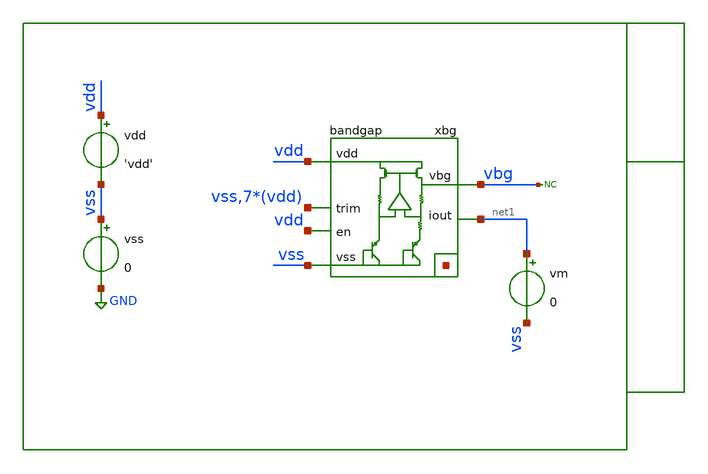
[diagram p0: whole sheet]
** sch_path: xschem/tb/bandgap_cm/bandgap/op_bandgap.sch
**.subckt op_bandgap
xbg vdd vbg vss net2[7] net2[6] net2[5] net2[4] net2[3] net2[2] net2[1] net2[0] vss vdd vdd vdd vdd
+ vdd vdd vdd net1 vdd bandgap
vdd vdd vss 'vdd'
vss vss GND 0
* noconn vbg
vm net1 vss 0
**** begin user architecture code

* Control

.param vdd = 3.3

.temp 27

.options reltol  = 1e-6
.options abstol  = 1e-12
.options gmin    = 1e-15

*------------------------------------------------------------
* Nodeset for better convergence
*------------------------------------------------------------
.nodeset v(vbg)  = '1'
.nodeset v(xbg.gate) = 'vdd/2'
.nodeset v(xbg.vx)   = '0.70'
.nodeset v(xbg.vbe2) = '0.65'
.nodeset v(xbg.vs1)  = '0'
*------------------------------------------------------------


.control

save all

* optran 0 0 0 100n 0.3m 0
op

let gm_xbg_xm2 = @m.xbg.xm2.m0[gm]
let gm_xbg_xms1 = @m.xbg.xms1.m0[gm]
let gm_xbg_xm1 = @m.xbg.xm1.m0[gm]
let gm_xbg_xmo1 = @m.xbg.xmo1.m0[gm]
let gm_xbg_xmb1 = @m.xbg.xmb1.m0[gm]
let gm_xbg_xmb2 = @m.xbg.xmb2.m0[gm]
let gm_xbg_xmb3 = @m.xbg.xmb3.m0[gm]
let gm_xbg_xmb2 = @m.xbg.xmb2.m0[gm]
let gm_xbg_xmb3 = @m.xbg.xmb3.m0[gm]
let gm_xbg_xmo2 = @m.xbg.xmo2.m0[gm]
let gm_xbg_xme1 = @m.xbg.xme1.m0[gm]
let gm_xbg_xme2 = @m.xbg.xme2.m0[gm]
let gm_xbg_xmi2 = @m.xbg.xmi2.m0[gm]
let gm_xbg_xmi1 = @m.xbg.xmi1.m0[gm]
let gm_xbg_xme3 = @m.xbg.xme3.m0[gm]
let gm_xbg_xme4 = @m.xbg.xme4.m0[gm]
let gm_xbg_xms2 = @m.xbg.xms2.m0[gm]
let gm_xbg_xms3 = @m.xbg.xms3.m0[gm]
let gm_xbg_xms4 = @m.xbg.xms4.m0[gm]
let gm_xamp_xmb1 = @m.xbg.xamp.xmb1.m0[gm]
let gm_xamp_xmb3 = @m.xbg.xamp.xmb3.m0[gm]
let gm_xamp_xmb2 = @m.xbg.xamp.xmb2.m0[gm]
let gm_xamp_xmd1 = @m.xbg.xamp.xmd1.m0[gm]
let gm_xamp_xmb4 = @m.xbg.xamp.xmb4.m0[gm]
let gm_xamp_xmb5 = @m.xbg.xamp.xmb5.m0[gm]
let gm_xamp_xmd2 = @m.xbg.xamp.xmd2.m0[gm]
let gm_xamp_xmt1 = @m.xbg.xamp.xmt1.m0[gm]
let gm_xamp_xmc7 = @m.xbg.xamp.xmc7.m0[gm]
let gm_xamp_xmc8 = @m.xbg.xamp.xmc8.m0[gm]
let gm_xamp_xmc1 = @m.xbg.xamp.xmc1.m0[gm]
let gm_xamp_xmc2 = @m.xbg.xamp.xmc2.m0[gm]
let gm_xamp_xmc3 = @m.xbg.xamp.xmc3.m0[gm]
let gm_xamp_xmc4 = @m.xbg.xamp.xmc4.m0[gm]
let gm_xamp_xmc5 = @m.xbg.xamp.xmc5.m0[gm]
let gm_xamp_xmc6 = @m.xbg.xamp.xmc6.m0[gm]
let gds_xbg_xm2 = @m.xbg.xm2.m0[gds]
let gds_xbg_xms1 = @m.xbg.xms1.m0[gds]
let gds_xbg_xm1 = @m.xbg.xm1.m0[gds]
let gds_xbg_xmo1 = @m.xbg.xmo1.m0[gds]
let gds_xbg_xmb1 = @m.xbg.xmb1.m0[gds]
let gds_xbg_xmb2 = @m.xbg.xmb2.m0[gds]
let gds_xbg_xmb3 = @m.xbg.xmb3.m0[gds]
let gds_xbg_xmb2 = @m.xbg.xmb2.m0[gds]
let gds_xbg_xmb3 = @m.xbg.xmb3.m0[gds]
let gds_xbg_xmo2 = @m.xbg.xmo2.m0[gds]
let gds_xbg_xme1 = @m.xbg.xme1.m0[gds]
let gds_xbg_xme2 = @m.xbg.xme2.m0[gds]
let gds_xbg_xmi2 = @m.xbg.xmi2.m0[gds]
let gds_xbg_xmi1 = @m.xbg.xmi1.m0[gds]
let gds_xbg_xme3 = @m.xbg.xme3.m0[gds]
let gds_xbg_xme4 = @m.xbg.xme4.m0[gds]
let gds_xbg_xms2 = @m.xbg.xms2.m0[gds]
let gds_xbg_xms3 = @m.xbg.xms3.m0[gds]
let gds_xbg_xms4 = @m.xbg.xms4.m0[gds]
let gds_xamp_xmb1 = @m.xbg.xamp.xmb1.m0[gds]
let gds_xamp_xmb3 = @m.xbg.xamp.xmb3.m0[gds]
let gds_xamp_xmb2 = @m.xbg.xamp.xmb2.m0[gds]
let gds_xamp_xmd1 = @m.xbg.xamp.xmd1.m0[gds]
let gds_xamp_xmb4 = @m.xbg.xamp.xmb4.m0[gds]
let gds_xamp_xmb5 = @m.xbg.xamp.xmb5.m0[gds]
let gds_xamp_xmd2 = @m.xbg.xamp.xmd2.m0[gds]
let gds_xamp_xmt1 = @m.xbg.xamp.xmt1.m0[gds]
let gds_xamp_xmc7 = @m.xbg.xamp.xmc7.m0[gds]
let gds_xamp_xmc8 = @m.xbg.xamp.xmc8.m0[gds]
let gds_xamp_xmc1 = @m.xbg.xamp.xmc1.m0[gds]
let gds_xamp_xmc2 = @m.xbg.xamp.xmc2.m0[gds]
let gds_xamp_xmc3 = @m.xbg.xamp.xmc3.m0[gds]
let gds_xamp_xmc4 = @m.xbg.xamp.xmc4.m0[gds]
let gds_xamp_xmc5 = @m.xbg.xamp.xmc5.m0[gds]
let gds_xamp_xmc6 = @m.xbg.xamp.xmc6.m0[gds]
let vdsat_xbg_xm2 = @m.xbg.xm2.m0[vdsat]
let vdsat_xbg_xms1 = @m.xbg.xms1.m0[vdsat]
let vdsat_xbg_xm1 = @m.xbg.xm1.m0[vdsat]
let vdsat_xbg_xmo1 = @m.xbg.xmo1.m0[vdsat]
let vdsat_xbg_xmb1 = @m.xbg.xmb1.m0[vdsat]
let vdsat_xbg_xmb2 = @m.xbg.xmb2.m0[vdsat]
let vdsat_xbg_xmb3 = @m.xbg.xmb3.m0[vdsat]
let vdsat_xbg_xmb2 = @m.xbg.xmb2.m0[vdsat]
let vdsat_xbg_xmb3 = @m.xbg.xmb3.m0[vdsat]
let vdsat_xbg_xmo2 = @m.xbg.xmo2.m0[vdsat]
let vdsat_xbg_xme1 = @m.xbg.xme1.m0[vdsat]
let vdsat_xbg_xme2 = @m.xbg.xme2.m0[vdsat]
let vdsat_xbg_xmi2 = @m.xbg.xmi2.m0[vdsat]
let vdsat_xbg_xmi1 = @m.xbg.xmi1.m0[vdsat]
let vdsat_xbg_xme3 = @m.xbg.xme3.m0[vdsat]
let vdsat_xbg_xme4 = @m.xbg.xme4.m0[vdsat]
let vdsat_xbg_xms2 = @m.xbg.xms2.m0[vdsat]
let vdsat_xbg_xms3 = @m.xbg.xms3.m0[vdsat]
let vdsat_xbg_xms4 = @m.xbg.xms4.m0[vdsat]
let vdsat_xamp_xmb1 = @m.xbg.xamp.xmb1.m0[vdsat]
let vdsat_xamp_xmb3 = @m.xbg.xamp.xmb3.m0[vdsat]
let vdsat_xamp_xmb2 = @m.xbg.xamp.xmb2.m0[vdsat]
let vdsat_xamp_xmd1 = @m.xbg.xamp.xmd1.m0[vdsat]
let vdsat_xamp_xmb4 = @m.xbg.xamp.xmb4.m0[vdsat]
let vdsat_xamp_xmb5 = @m.xbg.xamp.xmb5.m0[vdsat]
let vdsat_xamp_xmd2 = @m.xbg.xamp.xmd2.m0[vdsat]
let vdsat_xamp_xmt1 = @m.xbg.xamp.xmt1.m0[vdsat]
let vdsat_xamp_xmc7 = @m.xbg.xamp.xmc7.m0[vdsat]
let vdsat_xamp_xmc8 = @m.xbg.xamp.xmc8.m0[vdsat]
let vdsat_xamp_xmc1 = @m.xbg.xamp.xmc1.m0[vdsat]
let vdsat_xamp_xmc2 = @m.xbg.xamp.xmc2.m0[vdsat]
let vdsat_xamp_xmc3 = @m.xbg.xamp.xmc3.m0[vdsat]
let vdsat_xamp_xmc4 = @m.xbg.xamp.xmc4.m0[vdsat]
let vdsat_xamp_xmc5 = @m.xbg.xamp.xmc5.m0[vdsat]
let vdsat_xamp_xmc6 = @m.xbg.xamp.xmc6.m0[vdsat]
let vth_xbg_xm2 = @m.xbg.xm2.m0[vth]
let vth_xbg_xms1 = @m.xbg.xms1.m0[vth]
let vth_xbg_xm1 = @m.xbg.xm1.m0[vth]
let vth_xbg_xmo1 = @m.xbg.xmo1.m0[vth]
let vth_xbg_xmb1 = @m.xbg.xmb1.m0[vth]
let vth_xbg_xmb2 = @m.xbg.xmb2.m0[vth]
let vth_xbg_xmb3 = @m.xbg.xmb3.m0[vth]
let vth_xbg_xmb2 = @m.xbg.xmb2.m0[vth]
let vth_xbg_xmb3 = @m.xbg.xmb3.m0[vth]
let vth_xbg_xmo2 = @m.xbg.xmo2.m0[vth]
let vth_xbg_xme1 = @m.xbg.xme1.m0[vth]
let vth_xbg_xme2 = @m.xbg.xme2.m0[vth]
let vth_xbg_xmi2 = @m.xbg.xmi2.m0[vth]
let vth_xbg_xmi1 = @m.xbg.xmi1.m0[vth]
let vth_xbg_xme3 = @m.xbg.xme3.m0[vth]
let vth_xbg_xme4 = @m.xbg.xme4.m0[vth]
let vth_xbg_xms2 = @m.xbg.xms2.m0[vth]
let vth_xbg_xms3 = @m.xbg.xms3.m0[vth]
let vth_xbg_xms4 = @m.xbg.xms4.m0[vth]
let vth_xamp_xmb1 = @m.xbg.xamp.xmb1.m0[vth]
let vth_xamp_xmb3 = @m.xbg.xamp.xmb3.m0[vth]
let vth_xamp_xmb2 = @m.xbg.xamp.xmb2.m0[vth]
let vth_xamp_xmd1 = @m.xbg.xamp.xmd1.m0[vth]
let vth_xamp_xmb4 = @m.xbg.xamp.xmb4.m0[vth]
let vth_xamp_xmb5 = @m.xbg.xamp.xmb5.m0[vth]
let vth_xamp_xmd2 = @m.xbg.xamp.xmd2.m0[vth]
let vth_xamp_xmt1 = @m.xbg.xamp.xmt1.m0[vth]
let vth_xamp_xmc7 = @m.xbg.xamp.xmc7.m0[vth]
let vth_xamp_xmc8 = @m.xbg.xamp.xmc8.m0[vth]
let vth_xamp_xmc1 = @m.xbg.xamp.xmc1.m0[vth]
let vth_xamp_xmc2 = @m.xbg.xamp.xmc2.m0[vth]
let vth_xamp_xmc3 = @m.xbg.xamp.xmc3.m0[vth]
let vth_xamp_xmc4 = @m.xbg.xamp.xmc4.m0[vth]
let vth_xamp_xmc5 = @m.xbg.xamp.xmc5.m0[vth]
let vth_xamp_xmc6 = @m.xbg.xamp.xmc6.m0[vth]
let id_xbg_xm2 = @m.xbg.xm2.m0[id]
let id_xbg_xms1 = @m.xbg.xms1.m0[id]
let id_xbg_xm1 = @m.xbg.xm1.m0[id]
let id_xbg_xmo1 = @m.xbg.xmo1.m0[id]
let id_xbg_xmb1 = @m.xbg.xmb1.m0[id]
let id_xbg_xmb2 = @m.xbg.xmb2.m0[id]
let id_xbg_xmb3 = @m.xbg.xmb3.m0[id]
let id_xbg_xmb2 = @m.xbg.xmb2.m0[id]
let id_xbg_xmb3 = @m.xbg.xmb3.m0[id]
let id_xbg_xmo2 = @m.xbg.xmo2.m0[id]
let id_xbg_xme1 = @m.xbg.xme1.m0[id]
let id_xbg_xme2 = @m.xbg.xme2.m0[id]
let id_xbg_xmi2 = @m.xbg.xmi2.m0[id]
let id_xbg_xmi1 = @m.xbg.xmi1.m0[id]
let id_xbg_xme3 = @m.xbg.xme3.m0[id]
let id_xbg_xme4 = @m.xbg.xme4.m0[id]
let id_xbg_xms2 = @m.xbg.xms2.m0[id]
let id_xbg_xms3 = @m.xbg.xms3.m0[id]
let id_xbg_xms4 = @m.xbg.xms4.m0[id]
let id_xamp_xmb1 = @m.xbg.xamp.xmb1.m0[id]
let id_xamp_xmb3 = @m.xbg.xamp.xmb3.m0[id]
let id_xamp_xmb2 = @m.xbg.xamp.xmb2.m0[id]
let id_xamp_xmd1 = @m.xbg.xamp.xmd1.m0[id]
let id_xamp_xmb4 = @m.xbg.xamp.xmb4.m0[id]
let id_xamp_xmb5 = @m.xbg.xamp.xmb5.m0[id]
let id_xamp_xmd2 = @m.xbg.xamp.xmd2.m0[id]
let id_xamp_xmt1 = @m.xbg.xamp.xmt1.m0[id]
let id_xamp_xmc7 = @m.xbg.xamp.xmc7.m0[id]
let id_xamp_xmc8 = @m.xbg.xamp.xmc8.m0[id]
let id_xamp_xmc1 = @m.xbg.xamp.xmc1.m0[id]
let id_xamp_xmc2 = @m.xbg.xamp.xmc2.m0[id]
let id_xamp_xmc3 = @m.xbg.xamp.xmc3.m0[id]
let id_xamp_xmc4 = @m.xbg.xamp.xmc4.m0[id]
let id_xamp_xmc5 = @m.xbg.xamp.xmc5.m0[id]
let id_xamp_xmc6 = @m.xbg.xamp.xmc6.m0[id]
let vgs_xbg_xm2 = @m.xbg.xm2.m0[vgs]
let vgs_xbg_xms1 = @m.xbg.xms1.m0[vgs]
let vgs_xbg_xm1 = @m.xbg.xm1.m0[vgs]
let vgs_xbg_xmo1 = @m.xbg.xmo1.m0[vgs]
let vgs_xbg_xmb1 = @m.xbg.xmb1.m0[vgs]
let vgs_xbg_xmb2 = @m.xbg.xmb2.m0[vgs]
let vgs_xbg_xmb3 = @m.xbg.xmb3.m0[vgs]
let vgs_xbg_xmb2 = @m.xbg.xmb2.m0[vgs]
let vgs_xbg_xmb3 = @m.xbg.xmb3.m0[vgs]
let vgs_xbg_xmo2 = @m.xbg.xmo2.m0[vgs]
let vgs_xbg_xme1 = @m.xbg.xme1.m0[vgs]
let vgs_xbg_xme2 = @m.xbg.xme2.m0[vgs]
let vgs_xbg_xmi2 = @m.xbg.xmi2.m0[vgs]
let vgs_xbg_xmi1 = @m.xbg.xmi1.m0[vgs]
let vgs_xbg_xme3 = @m.xbg.xme3.m0[vgs]
let vgs_xbg_xme4 = @m.xbg.xme4.m0[vgs]
let vgs_xbg_xms2 = @m.xbg.xms2.m0[vgs]
let vgs_xbg_xms3 = @m.xbg.xms3.m0[vgs]
let vgs_xbg_xms4 = @m.xbg.xms4.m0[vgs]
let vgs_xamp_xmb1 = @m.xbg.xamp.xmb1.m0[vgs]
let vgs_xamp_xmb3 = @m.xbg.xamp.xmb3.m0[vgs]
let vgs_xamp_xmb2 = @m.xbg.xamp.xmb2.m0[vgs]
let vgs_xamp_xmd1 = @m.xbg.xamp.xmd1.m0[vgs]
let vgs_xamp_xmb4 = @m.xbg.xamp.xmb4.m0[vgs]
let vgs_xamp_xmb5 = @m.xbg.xamp.xmb5.m0[vgs]
let vgs_xamp_xmd2 = @m.xbg.xamp.xmd2.m0[vgs]
let vgs_xamp_xmt1 = @m.xbg.xamp.xmt1.m0[vgs]
let vgs_xamp_xmc7 = @m.xbg.xamp.xmc7.m0[vgs]
let vgs_xamp_xmc8 = @m.xbg.xamp.xmc8.m0[vgs]
let vgs_xamp_xmc1 = @m.xbg.xamp.xmc1.m0[vgs]
let vgs_xamp_xmc2 = @m.xbg.xamp.xmc2.m0[vgs]
let vgs_xamp_xmc3 = @m.xbg.xamp.xmc3.m0[vgs]
let vgs_xamp_xmc4 = @m.xbg.xamp.xmc4.m0[vgs]
let vgs_xamp_xmc5 = @m.xbg.xamp.xmc5.m0[vgs]
let vgs_xamp_xmc6 = @m.xbg.xamp.xmc6.m0[vgs]
let vds_xbg_xm2 = @m.xbg.xm2.m0[vds]
let vds_xbg_xms1 = @m.xbg.xms1.m0[vds]
let vds_xbg_xm1 = @m.xbg.xm1.m0[vds]
let vds_xbg_xmo1 = @m.xbg.xmo1.m0[vds]
let vds_xbg_xmb1 = @m.xbg.xmb1.m0[vds]
let vds_xbg_xmb2 = @m.xbg.xmb2.m0[vds]
let vds_xbg_xmb3 = @m.xbg.xmb3.m0[vds]
let vds_xbg_xmb2 = @m.xbg.xmb2.m0[vds]
let vds_xbg_xmb3 = @m.xbg.xmb3.m0[vds]
let vds_xbg_xmo2 = @m.xbg.xmo2.m0[vds]
let vds_xbg_xme1 = @m.xbg.xme1.m0[vds]
let vds_xbg_xme2 = @m.xbg.xme2.m0[vds]
let vds_xbg_xmi2 = @m.xbg.xmi2.m0[vds]
let vds_xbg_xmi1 = @m.xbg.xmi1.m0[vds]
let vds_xbg_xme3 = @m.xbg.xme3.m0[vds]
let vds_xbg_xme4 = @m.xbg.xme4.m0[vds]
let vds_xbg_xms2 = @m.xbg.xms2.m0[vds]
let vds_xbg_xms3 = @m.xbg.xms3.m0[vds]
let vds_xbg_xms4 = @m.xbg.xms4.m0[vds]
let vds_xamp_xmb1 = @m.xbg.xamp.xmb1.m0[vds]
let vds_xamp_xmb3 = @m.xbg.xamp.xmb3.m0[vds]
let vds_xamp_xmb2 = @m.xbg.xamp.xmb2.m0[vds]
let vds_xamp_xmd1 = @m.xbg.xamp.xmd1.m0[vds]
let vds_xamp_xmb4 = @m.xbg.xamp.xmb4.m0[vds]
let vds_xamp_xmb5 = @m.xbg.xamp.xmb5.m0[vds]
let vds_xamp_xmd2 = @m.xbg.xamp.xmd2.m0[vds]
let vds_xamp_xmt1 = @m.xbg.xamp.xmt1.m0[vds]
let vds_xamp_xmc7 = @m.xbg.xamp.xmc7.m0[vds]
let vds_xamp_xmc8 = @m.xbg.xamp.xmc8.m0[vds]
let vds_xamp_xmc1 = @m.xbg.xamp.xmc1.m0[vds]
let vds_xamp_xmc2 = @m.xbg.xamp.xmc2.m0[vds]
let vds_xamp_xmc3 = @m.xbg.xamp.xmc3.m0[vds]
let vds_xamp_xmc4 = @m.xbg.xamp.xmc4.m0[vds]
let vds_xamp_xmc5 = @m.xbg.xamp.xmc5.m0[vds]
let vds_xamp_xmc6 = @m.xbg.xamp.xmc6.m0[vds]

let vsat_xbg_xm2  = vds_xbg_xm2  - vdsat_xbg_xm2
let vsat_xbg_xms1 = vds_xbg_xms1 - vdsat_xbg_xms1
let vsat_xbg_xm1  = vds_xbg_xm1  - vdsat_xbg_xm1
let vsat_xbg_xmo1 = vds_xbg_xmo1 - vdsat_xbg_xmo1
let vsat_xbg_xmb1 = vds_xbg_xmb1 - vdsat_xbg_xmb1
let vsat_xbg_xmb2 = vds_xbg_xmb2 - vdsat_xbg_xmb2
let vsat_xbg_xmb3 = vds_xbg_xmb3 - vdsat_xbg_xmb3
let vsat_xbg_xmb2 = vds_xbg_xmb2 - vdsat_xbg_xmb2
let vsat_xbg_xmb3 = vds_xbg_xmb3 - vdsat_xbg_xmb3
let vsat_xbg_xmo2 = vds_xbg_xmo2 - vdsat_xbg_xmo2
let vsat_xbg_xme1 = vds_xbg_xme1 - vdsat_xbg_xme1
let vsat_xbg_xme2 = vds_xbg_xme2 - vdsat_xbg_xme2
let vsat_xbg_xmi2 = vds_xbg_xmi2 - vdsat_xbg_xmi2
let vsat_xbg_xmi1 = vds_xbg_xmi1 - vdsat_xbg_xmi1
let vsat_xbg_xme3 = vds_xbg_xme3 - vdsat_xbg_xme3
let vsat_xbg_xme4 = vds_xbg_xme4 - vdsat_xbg_xme4
let vsat_xbg_xms2 = vds_xbg_xms2 - vdsat_xbg_xms2
let vsat_xbg_xms3 = vds_xbg_xms3 - vdsat_xbg_xms3
let vsat_xbg_xms4 = vds_xbg_xms4 - vdsat_xbg_xms4
let vsat_xamp_xmb1 = vds_xamp_xmb1 - vdsat_xamp_xmb1
let vsat_xamp_xmb3 = vds_xamp_xmb3 - vdsat_xamp_xmb3
let vsat_xamp_xmb2 = vds_xamp_xmb2 - vdsat_xamp_xmb2
let vsat_xamp_xmd1 = vds_xamp_xmd1 - vdsat_xamp_xmd1
let vsat_xamp_xmb4 = vds_xamp_xmb4 - vdsat_xamp_xmb4
let vsat_xamp_xmb5 = vds_xamp_xmb5 - vdsat_xamp_xmb5
let vsat_xamp_xmd2 = vds_xamp_xmd2 - vdsat_xamp_xmd2
let vsat_xamp_xmt1 = vds_xamp_xmt1 - vdsat_xamp_xmt1
let vsat_xamp_xmc7 = vds_xamp_xmc7 - vdsat_xamp_xmc7
let vsat_xamp_xmc8 = vds_xamp_xmc8 - vdsat_xamp_xmc8
let vsat_xamp_xmc1 = vds_xamp_xmc1 - vdsat_xamp_xmc1
let vsat_xamp_xmc2 = vds_xamp_xmc2 - vdsat_xamp_xmc2
let vsat_xamp_xmc3 = vds_xamp_xmc3 - vdsat_xamp_xmc3
let vsat_xamp_xmc4 = vds_xamp_xmc4 - vdsat_xamp_xmc4
let vsat_xamp_xmc5 = vds_xamp_xmc5 - vdsat_xamp_xmc5
let vsat_xamp_xmc6 = vds_xamp_xmc6 - vdsat_xamp_xmc6

let vov_xbg_xm2  = vgs_xbg_xm2  - vth_xbg_xm2
let vov_xbg_xms1 = vgs_xbg_xms1 - vth_xbg_xms1
let vov_xbg_xm1  = vgs_xbg_xm1  - vth_xbg_xm1
let vov_xbg_xmo1 = vgs_xbg_xmo1 - vth_xbg_xmo1
let vov_xbg_xmb1 = vgs_xbg_xmb1 - vth_xbg_xmb1
let vov_xbg_xmb2 = vgs_xbg_xmb2 - vth_xbg_xmb2
let vov_xbg_xmb3 = vgs_xbg_xmb3 - vth_xbg_xmb3
let vov_xbg_xmb2 = vgs_xbg_xmb2 - vth_xbg_xmb2
let vov_xbg_xmb3 = vgs_xbg_xmb3 - vth_xbg_xmb3
let vov_xbg_xmo2 = vgs_xbg_xmo2 - vth_xbg_xmo2
let vov_xbg_xme1 = vgs_xbg_xme1 - vth_xbg_xme1
let vov_xbg_xme2 = vgs_xbg_xme2 - vth_xbg_xme2
let vov_xbg_xmi2 = vgs_xbg_xmi2 - vth_xbg_xmi2
let vov_xbg_xmi1 = vgs_xbg_xmi1 - vth_xbg_xmi1
let vov_xbg_xme3 = vgs_xbg_xme3 - vth_xbg_xme3
let vov_xbg_xme4 = vgs_xbg_xme4 - vth_xbg_xme4
let vov_xbg_xms2 = vgs_xbg_xms2 - vth_xbg_xms2
let vov_xbg_xms3 = vgs_xbg_xms3 - vth_xbg_xms3
let vov_xbg_xms4 = vgs_xbg_xms4 - vth_xbg_xms4
let vov_xamp_xmb1 = vgs_xamp_xmb1 - vth_xamp_xmb1
let vov_xamp_xmb3 = vgs_xamp_xmb3 - vth_xamp_xmb3
let vov_xamp_xmb2 = vgs_xamp_xmb2 - vth_xamp_xmb2
let vov_xamp_xmd1 = vgs_xamp_xmd1 - vth_xamp_xmd1
let vov_xamp_xmb4 = vgs_xamp_xmb4 - vth_xamp_xmb4
let vov_xamp_xmb5 = vgs_xamp_xmb5 - vth_xamp_xmb5
let vov_xamp_xmd2 = vgs_xamp_xmd2 - vth_xamp_xmd2
let vov_xamp_xmt1 = vgs_xamp_xmt1 - vth_xamp_xmt1
let vov_xamp_xmc7 = vgs_xamp_xmc7 - vth_xamp_xmc7
let vov_xamp_xmc8 = vgs_xamp_xmc8 - vth_xamp_xmc8
let vov_xamp_xmc1 = vgs_xamp_xmc1 - vth_xamp_xmc1
let vov_xamp_xmc2 = vgs_xamp_xmc2 - vth_xamp_xmc2
let vov_xamp_xmc3 = vgs_xamp_xmc3 - vth_xamp_xmc3
let vov_xamp_xmc4 = vgs_xamp_xmc4 - vth_xamp_xmc4
let vov_xamp_xmc5 = vgs_xamp_xmc5 - vth_xamp_xmc5
let vov_xamp_xmc6 = vgs_xamp_xmc6 - vth_xamp_xmc6



let ie_xq1 = abs(v.xbg.vmbjt1#branch)
let ie_xq2 = abs(v.xbg.vmbjt2#branch)
let i_amp = abs(v.xbg.vmamp#branch)
let i_xm1 = abs(v.xbg.vmxm1#branch)
let i_xm2 = abs(v.xbg.vmxm2#branch)
let i_r1 = ie_xq2
let i_r3 = abs(v.xbg.vmr3#branch)
let i_r2 = abs(v.xbg.vmr2#branch)
let iout = abs(vm#branch)

print vbg
print iout

print gm_xbg_xm2
print gm_xbg_xms1
print gm_xbg_xm1
print gm_xbg_xmo1
print gm_xbg_xmb1
print gm_xbg_xmb2
print gm_xbg_xmb3
print gm_xbg_xmb2
print gm_xbg_xmb3
print gm_xbg_xmo2
print gm_xbg_xme1
print gm_xbg_xme2
print gm_xbg_xmi2
print gm_xbg_xmi1
print gm_xbg_xme3
print gm_xbg_xme4
print gm_xbg_xms2
print gm_xbg_xms3
print gm_xbg_xms4
print gm_xamp_xmb1
print gm_xamp_xmb3
print gm_xamp_xmb2
print gm_xamp_xmd1
print gm_xamp_xmb4
print gm_xamp_xmb5
print gm_xamp_xmd2
print gm_xamp_xmt1
print gm_xamp_xmc7
print gm_xamp_xmc8
print gm_xamp_xmc1
print gm_xamp_xmc2
print gm_xamp_xmc3
print gm_xamp_xmc4
print gm_xamp_xmc5
print gm_xamp_xmc6
print gds_xbg_xm2
print gds_xbg_xms1
print gds_xbg_xm1
print gds_xbg_xmo1
print gds_xbg_xmb1
print gds_xbg_xmb2
print gds_xbg_xmb3
print gds_xbg_xmb2
print gds_xbg_xmb3
print gds_xbg_xmo2
print gds_xbg_xme1
print gds_xbg_xme2
print gds_xbg_xmi2
print gds_xbg_xmi1
print gds_xbg_xme3
print gds_xbg_xme4
print gds_xbg_xms2
print gds_xbg_xms3
print gds_xbg_xms4
print gds_xamp_xmb1
print gds_xamp_xmb3
print gds_xamp_xmb2
print gds_xamp_xmd1
print gds_xamp_xmb4
print gds_xamp_xmb5
print gds_xamp_xmd2
print gds_xamp_xmt1
print gds_xamp_xmc7
print gds_xamp_xmc8
print gds_xamp_xmc1
print gds_xamp_xmc2
print gds_xamp_xmc3
print gds_xamp_xmc4
print gds_xamp_xmc5
print gds_xamp_xmc6
print vdsat_xbg_xm2
print vdsat_xbg_xms1
print vdsat_xbg_xm1
print vdsat_xbg_xmo1
print vdsat_xbg_xmb1
print vdsat_xbg_xmb2
print vdsat_xbg_xmb3
print vdsat_xbg_xmb2
print vdsat_xbg_xmb3
print vdsat_xbg_xmo2
print vdsat_xbg_xme1
print vdsat_xbg_xme2
print vdsat_xbg_xmi2
print vdsat_xbg_xmi1
print vdsat_xbg_xme3
print vdsat_xbg_xme4
print vdsat_xbg_xms2
print vdsat_xbg_xms3
print vdsat_xbg_xms4
print vdsat_xamp_xmb1
print vdsat_xamp_xmb3
print vdsat_xamp_xmb2
print vdsat_xamp_xmd1
print vdsat_xamp_xmb4
print vdsat_xamp_xmb5
print vdsat_xamp_xmd2
print vdsat_xamp_xmt1
print vdsat_xamp_xmc7
print vdsat_xamp_xmc8
print vdsat_xamp_xmc1
print vdsat_xamp_xmc2
print vdsat_xamp_xmc3
print vdsat_xamp_xmc4
print vdsat_xamp_xmc5
print vdsat_xamp_xmc6
print vth_xbg_xm2
print vth_xbg_xms1
print vth_xbg_xm1
print vth_xbg_xmo1
print vth_xbg_xmb1
print vth_xbg_xmb2
print vth_xbg_xmb3
print vth_xbg_xmb2
print vth_xbg_xmb3
print vth_xbg_xmo2
print vth_xbg_xme1
print vth_xbg_xme2
print vth_xbg_xmi2
print vth_xbg_xmi1
print vth_xbg_xme3
print vth_xbg_xme4
print vth_xbg_xms2
print vth_xbg_xms3
print vth_xbg_xms4
print vth_xamp_xmb1
print vth_xamp_xmb3
print vth_xamp_xmb2
print vth_xamp_xmd1
print vth_xamp_xmb4
print vth_xamp_xmb5
print vth_xamp_xmd2
print vth_xamp_xmt1
print vth_xamp_xmc7
print vth_xamp_xmc8
print vth_xamp_xmc1
print vth_xamp_xmc2
print vth_xamp_xmc3
print vth_xamp_xmc4
print vth_xamp_xmc5
print vth_xamp_xmc6
print id_xbg_xm2
print id_xbg_xms1
print id_xbg_xm1
print id_xbg_xmo1
print id_xbg_xmb1
print id_xbg_xmb2
print id_xbg_xmb3
print id_xbg_xmb2
print id_xbg_xmb3
print id_xbg_xmo2
print id_xbg_xme1
print id_xbg_xme2
print id_xbg_xmi2
print id_xbg_xmi1
print id_xbg_xme3
print id_xbg_xme4
print id_xbg_xms2
print id_xbg_xms3
print id_xbg_xms4
print id_xamp_xmb1
print id_xamp_xmb3
print id_xamp_xmb2
print id_xamp_xmd1
print id_xamp_xmb4
print id_xamp_xmb5
print id_xamp_xmd2
print id_xamp_xmt1
print id_xamp_xmc7
print id_xamp_xmc8
print id_xamp_xmc1
print id_xamp_xmc2
print id_xamp_xmc3
print id_xamp_xmc4
print id_xamp_xmc5
print id_xamp_xmc6
print vgs_xbg_xm2
print vgs_xbg_xms1
print vgs_xbg_xm1
print vgs_xbg_xmo1
print vgs_xbg_xmb1
print vgs_xbg_xmb2
print vgs_xbg_xmb3
print vgs_xbg_xmb2
print vgs_xbg_xmb3
print vgs_xbg_xmo2
print vgs_xbg_xme1
print vgs_xbg_xme2
print vgs_xbg_xmi2
print vgs_xbg_xmi1
print vgs_xbg_xme3
print vgs_xbg_xme4
print vgs_xbg_xms2
print vgs_xbg_xms3
print vgs_xbg_xms4
print vgs_xamp_xmb1
print vgs_xamp_xmb3
print vgs_xamp_xmb2
print vgs_xamp_xmd1
print vgs_xamp_xmb4
print vgs_xamp_xmb5
print vgs_xamp_xmd2
print vgs_xamp_xmt1
print vgs_xamp_xmc7
print vgs_xamp_xmc8
print vgs_xamp_xmc1
print vgs_xamp_xmc2
print vgs_xamp_xmc3
print vgs_xamp_xmc4
print vgs_xamp_xmc5
print vgs_xamp_xmc6
print vds_xbg_xm2
print vds_xbg_xms1
print vds_xbg_xm1
print vds_xbg_xmo1
print vds_xbg_xmb1
print vds_xbg_xmb2
print vds_xbg_xmb3
print vds_xbg_xmb2
print vds_xbg_xmb3
print vds_xbg_xmo2
print vds_xbg_xme1
print vds_xbg_xme2
print vds_xbg_xmi2
print vds_xbg_xmi1
print vds_xbg_xme3
print vds_xbg_xme4
print vds_xbg_xms2
print vds_xbg_xms3
print vds_xbg_xms4
print vds_xamp_xmb1
print vds_xamp_xmb3
print vds_xamp_xmb2
print vds_xamp_xmd1
print vds_xamp_xmb4
print vds_xamp_xmb5
print vds_xamp_xmd2
print vds_xamp_xmt1
print vds_xamp_xmc7
print vds_xamp_xmc8
print vds_xamp_xmc1
print vds_xamp_xmc2
print vds_xamp_xmc3
print vds_xamp_xmc4
print vds_xamp_xmc5
print vds_xamp_xmc6
print vsat_xbg_xm2
print vsat_xbg_xms1
print vsat_xbg_xm1
print vsat_xbg_xmo1
print vsat_xbg_xmb1
print vsat_xbg_xmb2
print vsat_xbg_xmb3
print vsat_xbg_xmb2
print vsat_xbg_xmb3
print vsat_xbg_xmo2
print vsat_xbg_xme1
print vsat_xbg_xme2
print vsat_xbg_xmi2
print vsat_xbg_xmi1
print vsat_xbg_xme3
print vsat_xbg_xme4
print vsat_xbg_xms2
print vsat_xbg_xms3
print vsat_xbg_xms4
print vsat_xamp_xmb1
print vsat_xamp_xmb3
print vsat_xamp_xmb2
print vsat_xamp_xmd1
print vsat_xamp_xmb4
print vsat_xamp_xmb5
print vsat_xamp_xmd2
print vsat_xamp_xmt1
print vsat_xamp_xmc7
print vsat_xamp_xmc8
print vsat_xamp_xmc1
print vsat_xamp_xmc2
print vsat_xamp_xmc3
print vsat_xamp_xmc4
print vsat_xamp_xmc5
print vsat_xamp_xmc6
print vov_xbg_xm2
print vov_xbg_xms1
print vov_xbg_xm1
print vov_xbg_xmo1
print vov_xbg_xmb1
print vov_xbg_xmb2
print vov_xbg_xmb3
print vov_xbg_xmb2
print vov_xbg_xmb3
print vov_xbg_xmo2
print vov_xbg_xme1
print vov_xbg_xme2
print vov_xbg_xmi2
print vov_xbg_xmi1
print vov_xbg_xme3
print vov_xbg_xme4
print vov_xbg_xms2
print vov_xbg_xms3
print vov_xbg_xms4
print vov_xamp_xmb1
print vov_xamp_xmb3
print vov_xamp_xmb2
print vov_xamp_xmd1
print vov_xamp_xmb4
print vov_xamp_xmb5
print vov_xamp_xmd2
print vov_xamp_xmt1
print vov_xamp_xmc7
print vov_xamp_xmc8
print vov_xamp_xmc1
print vov_xamp_xmc2
print vov_xamp_xmc3
print vov_xamp_xmc4
print vov_xamp_xmc5
print vov_xamp_xmc6
print ie_xq1
print ie_xq2
print i_amp
print i_xm1
print i_xm2
print i_r1
print i_r3
print i_r2
print iout

write op_bandgap.raw

.endc
.end


 * Model Corners

.include $::CORNERS/ngspice/tt.spice
*.include $::CORNERS/ngspice/ff.spice
*.include $::CORNERS/ngspice/ss.spice
*.include $::CORNERS/ngspice/sf.spice
*.include $::CORNERS/ngspice/fs.spice

**** end user architecture code
**.ends
.GLOBAL GND
.end
